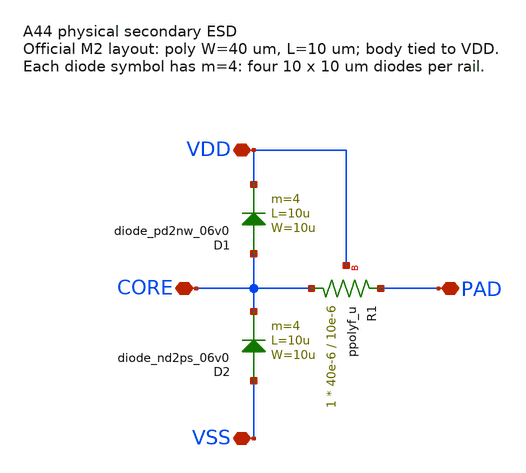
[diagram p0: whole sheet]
** sch_path: verification/a44_q2_analog_esd/schematic/A44_SECONDARY_ESD_M2_SCHEM.sch
**.subckt A44_SECONDARY_ESD_M2_SCHEM VSS VDD CORE PAD
*.iopin VSS
*.iopin VDD
*.iopin CORE
*.iopin PAD
D1 CORE VDD diode_pd2nw_06v0 area='10u * 10u ' pj='2*10u + 2*10u ' m=4
XR1 CORE PAD VDD ppolyf_u r_width=40e-6 r_length=10e-6 m=1
D2 VSS CORE diode_nd2ps_06v0 area='10u * 10u ' pj='2*10u + 2*10u ' m=4
**.ends
.end
